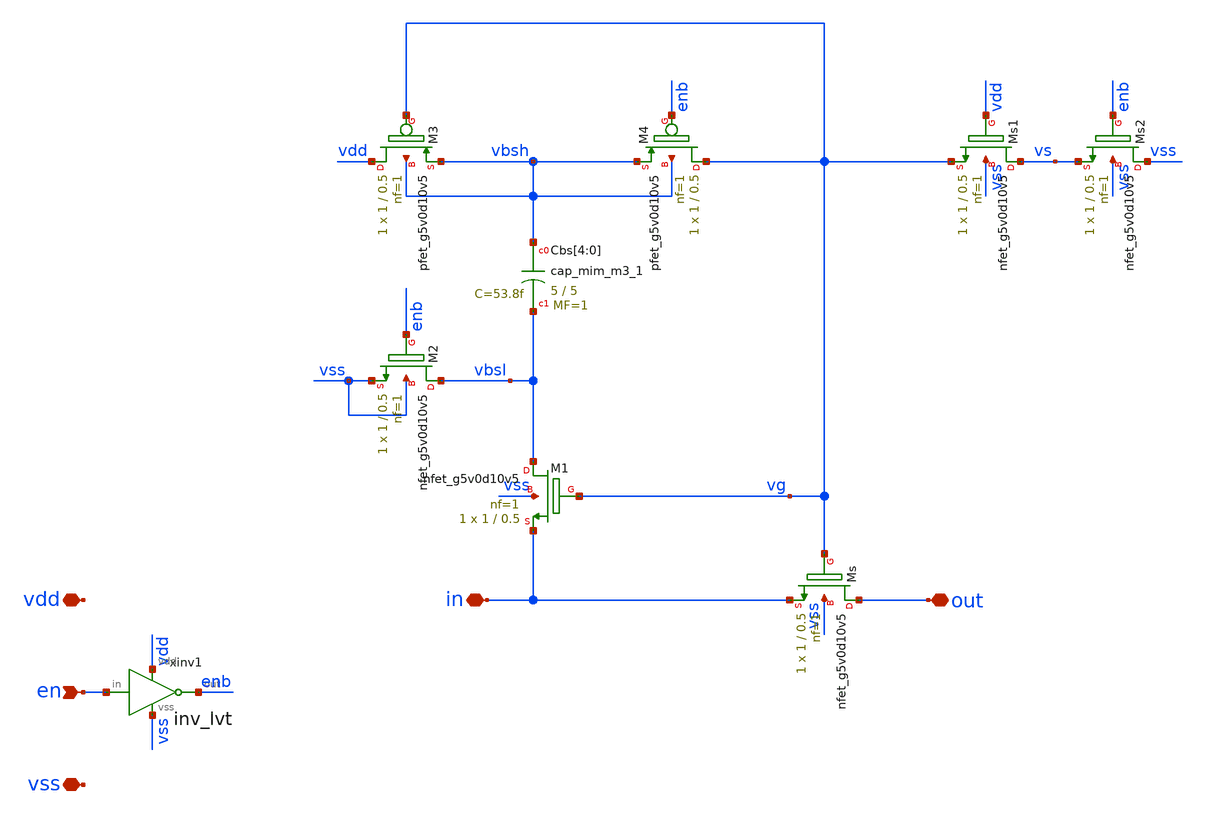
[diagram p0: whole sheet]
** sch_path: xschem/switches/bootstrapped_sw_hv.sch
**.subckt bootstrapped_sw_hv out en vss vdd in
*.iopin out
*.ipin en
*.iopin vss
*.iopin vdd
*.iopin in
xinv1 vdd en enb vss inv_lvt
XCbs[4] vbsh vbsl sky130_fd_pr__cap_mim_m3_1 W=5 L=5 MF=1 m=1
XCbs[3] vbsh vbsl sky130_fd_pr__cap_mim_m3_1 W=5 L=5 MF=1 m=1
XCbs[2] vbsh vbsl sky130_fd_pr__cap_mim_m3_1 W=5 L=5 MF=1 m=1
XCbs[1] vbsh vbsl sky130_fd_pr__cap_mim_m3_1 W=5 L=5 MF=1 m=1
XCbs[0] vbsh vbsl sky130_fd_pr__cap_mim_m3_1 W=5 L=5 MF=1 m=1
XM3 vdd vg vbsh vbsh sky130_fd_pr__pfet_g5v0d10v5 L=0.5 W=1 nf=1 ad='int((nf+1)/2) * W/nf * 0.29' as='int((nf+2)/2) * W/nf * 0.29'
+ pd='2*int((nf+1)/2) * (W/nf + 0.29)' ps='2*int((nf+2)/2) * (W/nf + 0.29)' nrd='0.29 / W' nrs='0.29 / W'
+ sa=0 sb=0 sd=0 mult=1 m=1
XM4 vg enb vbsh vbsh sky130_fd_pr__pfet_g5v0d10v5 L=0.5 W=1 nf=1 ad='int((nf+1)/2) * W/nf * 0.29' as='int((nf+2)/2) * W/nf * 0.29'
+ pd='2*int((nf+1)/2) * (W/nf + 0.29)' ps='2*int((nf+2)/2) * (W/nf + 0.29)' nrd='0.29 / W' nrs='0.29 / W'
+ sa=0 sb=0 sd=0 mult=1 m=1
XMs out vg in vss sky130_fd_pr__nfet_g5v0d10v5 L=0.5 W=1 nf=1 ad='int((nf+1)/2) * W/nf * 0.29' as='int((nf+2)/2) * W/nf * 0.29'
+ pd='2*int((nf+1)/2) * (W/nf + 0.29)' ps='2*int((nf+2)/2) * (W/nf + 0.29)' nrd='0.29 / W' nrs='0.29 / W'
+ sa=0 sb=0 sd=0 mult=1 m=1
XM1 vbsl vg in vss sky130_fd_pr__nfet_g5v0d10v5 L=0.5 W=1 nf=1 ad='int((nf+1)/2) * W/nf * 0.29' as='int((nf+2)/2) * W/nf * 0.29'
+ pd='2*int((nf+1)/2) * (W/nf + 0.29)' ps='2*int((nf+2)/2) * (W/nf + 0.29)' nrd='0.29 / W' nrs='0.29 / W'
+ sa=0 sb=0 sd=0 mult=1 m=1
XM2 vbsl enb vss vss sky130_fd_pr__nfet_g5v0d10v5 L=0.5 W=1 nf=1 ad='int((nf+1)/2) * W/nf * 0.29' as='int((nf+2)/2) * W/nf * 0.29'
+ pd='2*int((nf+1)/2) * (W/nf + 0.29)' ps='2*int((nf+2)/2) * (W/nf + 0.29)' nrd='0.29 / W' nrs='0.29 / W'
+ sa=0 sb=0 sd=0 mult=1 m=1
XMs2 vss enb vs vss sky130_fd_pr__nfet_g5v0d10v5 L=0.5 W=1 nf=1 ad='int((nf+1)/2) * W/nf * 0.29' as='int((nf+2)/2) * W/nf * 0.29'
+ pd='2*int((nf+1)/2) * (W/nf + 0.29)' ps='2*int((nf+2)/2) * (W/nf + 0.29)' nrd='0.29 / W' nrs='0.29 / W'
+ sa=0 sb=0 sd=0 mult=1 m=1
XMs1 vs vdd vg vss sky130_fd_pr__nfet_g5v0d10v5 L=0.5 W=1 nf=1 ad='int((nf+1)/2) * W/nf * 0.29' as='int((nf+2)/2) * W/nf * 0.29'
+ pd='2*int((nf+1)/2) * (W/nf + 0.29)' ps='2*int((nf+2)/2) * (W/nf + 0.29)' nrd='0.29 / W' nrs='0.29 / W'
+ sa=0 sb=0 sd=0 mult=1 m=1
**.ends

* expanding   symbol:  logic/inv_lvt.sym # of pins=4
** sym_path: xschem/logic/inv_lvt.sym
** sch_path: xschem/logic/inv_lvt.sch
.subckt inv_lvt vdd in out vss
*.iopin vdd
*.iopin vss
*.ipin in
*.opin out
XM1 out in vss vss sky130_fd_pr__nfet_01v8_lvt L=0.4 W=1 nf=1 ad='int((nf+1)/2) * W/nf * 0.29' as='int((nf+2)/2) * W/nf * 0.29'
+ pd='2*int((nf+1)/2) * (W/nf + 0.29)' ps='2*int((nf+2)/2) * (W/nf + 0.29)' nrd='0.29 / W' nrs='0.29 / W'
+ sa=0 sb=0 sd=0 mult=1 m=1
XM2 out in vdd vdd sky130_fd_pr__pfet_01v8_lvt L=0.4 W=1 nf=1 ad='int((nf+1)/2) * W/nf * 0.29' as='int((nf+2)/2) * W/nf * 0.29'
+ pd='2*int((nf+1)/2) * (W/nf + 0.29)' ps='2*int((nf+2)/2) * (W/nf + 0.29)' nrd='0.29 / W' nrs='0.29 / W'
+ sa=0 sb=0 sd=0 mult=1 m=1
.ends

.end
